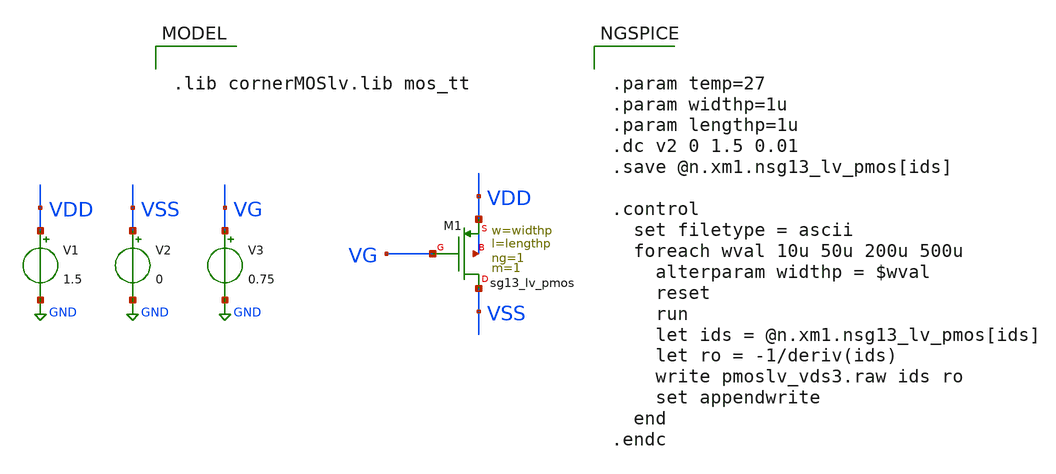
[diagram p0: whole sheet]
** sch_path: analog/tb/tb_pmos_lv_vds.sch
**.subckt tb_pmos_lv_vds
V1 VDD GND 1.5
V2 VSS GND 0
V3 VG GND 0.75
XM1 VSS VG VDD VDD sg13_lv_pmos w=widthp l=lengthp ng=1 m=1 mm_ok=1
**** begin user architecture code


.param temp=27
.param widthp=1u
.param lengthp=1u
.dc v2 0 1.5 0.01
.save @n.xm1.nsg13_lv_pmos[ids]

.control
  set filetype = ascii
  foreach wval 10u 50u 200u 500u
    alterparam widthp = $wval
    reset
    run
    let ids = @n.xm1.nsg13_lv_pmos[ids]
    let ro = -1/deriv(ids)
    write pmoslv_vds3.raw ids ro
    set appendwrite
  end
.endc





.lib cornerMOSlv.lib mos_tt


**** end user architecture code
**.ends
.GLOBAL GND
.end
